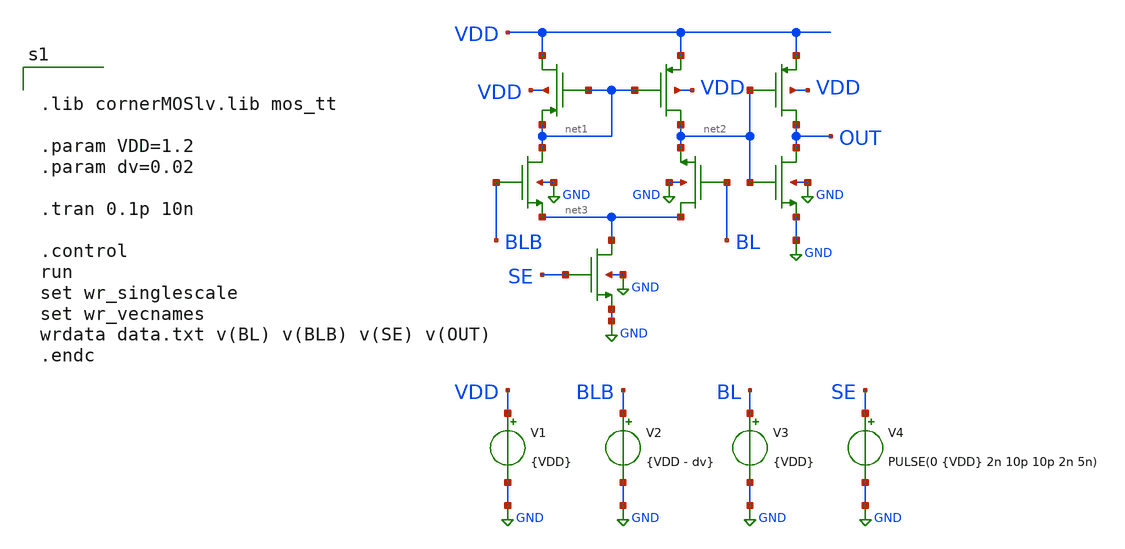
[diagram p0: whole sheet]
** sch_path: xschem/sram-sense-amp.sch
**.subckt sram-sense-amp
V1 VDD GND {VDD}
V2 BLB GND {VDD - dv}
V3 BL GND {VDD}
V4 SE GND PULSE(0 {VDD} 2n 10p 10p 2n 5n)
XM8 net3 SE GND GND sg13_lv_nmos w=0.15u l=0.13u ng=1 m=1 mm_ok=1
XM9 OUT net2 VDD VDD sg13_lv_pmos w=0.15u l=0.13u ng=1 m=1 mm_ok=1
XM1 net1 BLB net3 GND sg13_lv_nmos w=0.15u l=0.13u ng=1 m=1 mm_ok=1
XM4 net3 BL net2 GND sg13_lv_nmos w=0.15u l=0.13u ng=1 m=1 mm_ok=1
XM3 net2 net1 VDD VDD sg13_lv_pmos w=0.15u l=0.13u ng=1 m=1 mm_ok=1
XM2 VDD net1 net1 VDD sg13_lv_pmos w=0.15u l=0.13u ng=1 m=1 mm_ok=1
XM6 OUT net2 GND GND sg13_lv_nmos w=0.15u l=0.13u ng=1 m=1 mm_ok=1
**** begin user architecture code


.lib cornerMOSlv.lib mos_tt

.param VDD=1.2
.param dv=0.02

.tran 0.1p 10n

.control
run
set wr_singlescale
set wr_vecnames
wrdata data.txt v(BL) v(BLB) v(SE) v(OUT)
.endc


**** end user architecture code
**.ends
.GLOBAL GND
.end
